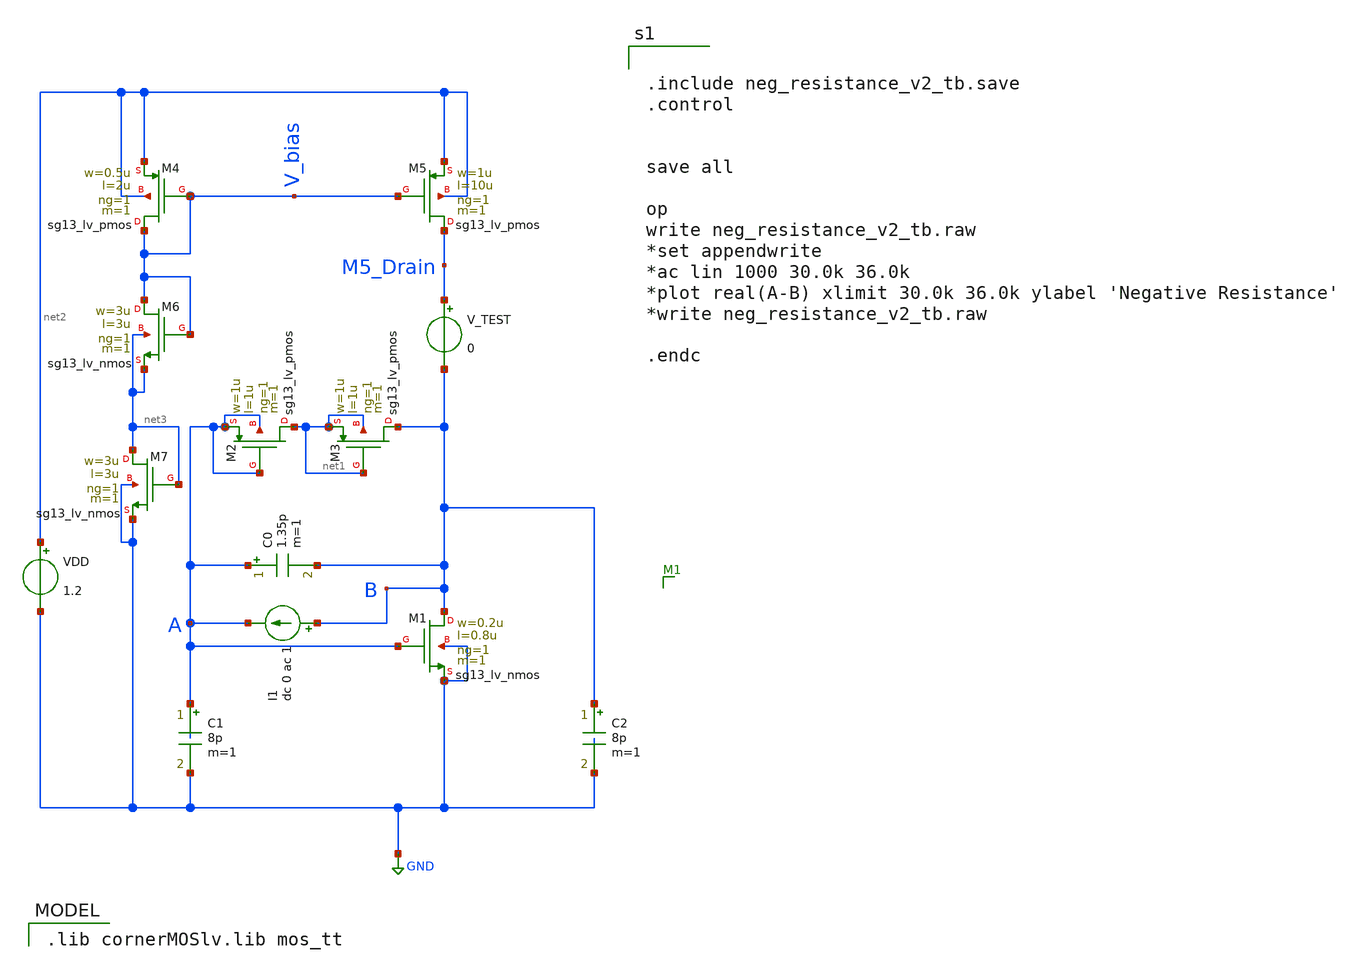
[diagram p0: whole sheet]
** sch_path: neg_resistance_v2_tb.sch
**.subckt neg_resistance_v2_tb
XM1 B A GND GND sg13_lv_nmos w=0.2u l=0.8u ng=1 m=1 mm_ok=1
C1 A GND 8p m=1
C2 B GND 8p m=1
C0 A B 1.35p m=1
VDD net2 GND 1.2
I1 B A dc 0 ac 1
XM2 net1 A A A sg13_lv_pmos w=1u l=1u ng=1 m=1 mm_ok=1
XM3 B net1 net1 net1 sg13_lv_pmos w=1u l=1u ng=1 m=1 mm_ok=1
XM4 V_bias V_bias net2 net2 sg13_lv_pmos w=0.5u l=2u ng=1 m=1 mm_ok=1
XM5 M5_Drain V_bias net2 net2 sg13_lv_pmos w=1u l=10u ng=1 m=1 mm_ok=1
XM6 V_bias V_bias net3 net3 sg13_lv_nmos w=3u l=3u ng=1 m=1 mm_ok=1
XM7 net3 net3 GND GND sg13_lv_nmos w=3u l=3u ng=1 m=1 mm_ok=1
V_TEST M5_Drain B 0
**** begin user architecture code


.include neg_resistance_v2_tb.save
.control


save all

op
write neg_resistance_v2_tb.raw
*set appendwrite
*ac lin 1000 30.0k 36.0k
*plot real(A-B) xlimit 30.0k 36.0k ylabel 'Negative Resistance'
*write neg_resistance_v2_tb.raw

.endc


 .lib cornerMOSlv.lib mos_tt

**** end user architecture code
**.ends
.GLOBAL GND
.end
